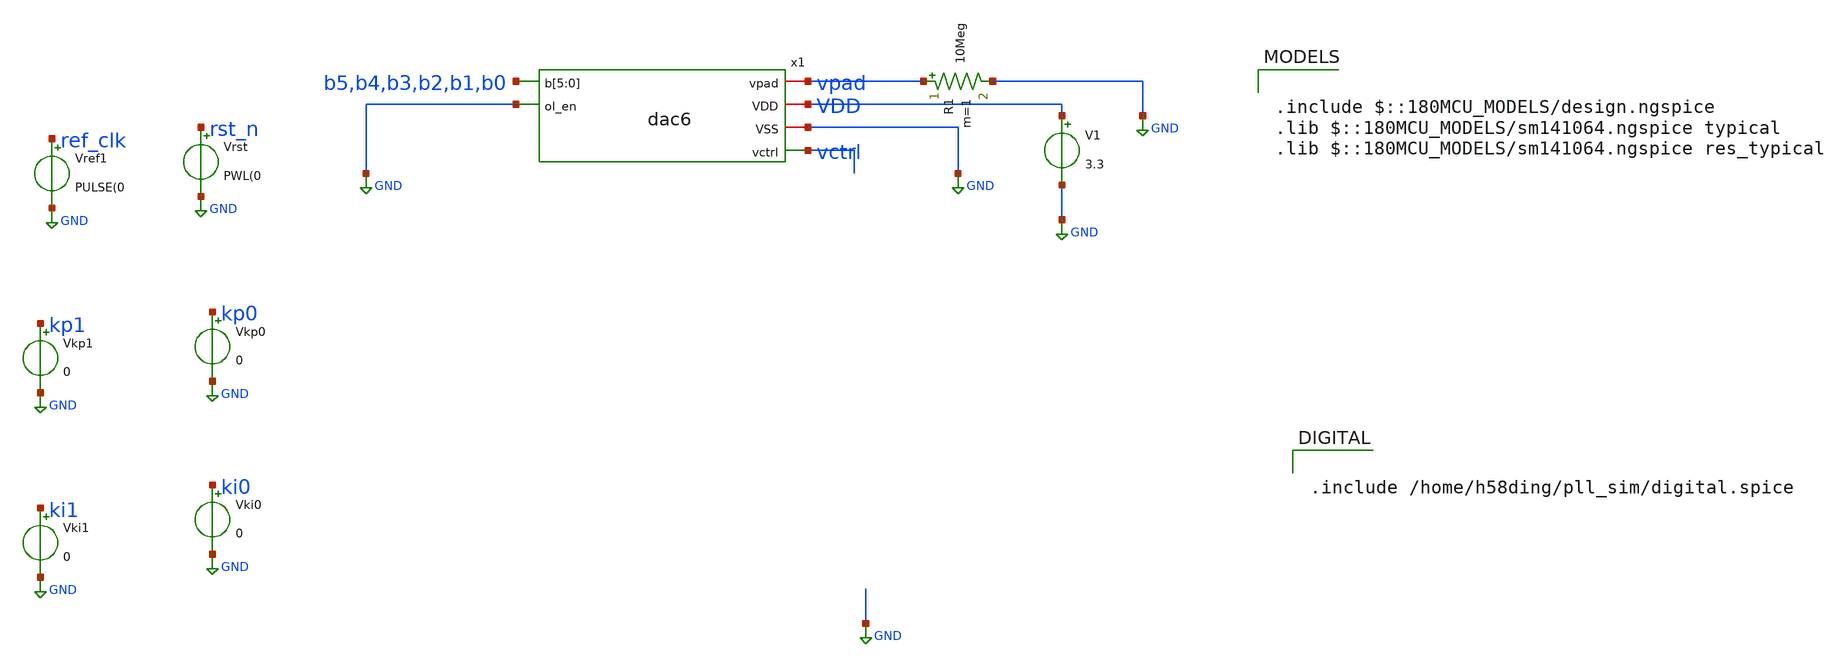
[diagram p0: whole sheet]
** sch_path: xschem/pll_dac/tb_pll.sch
**.subckt tb_pll
x1 b5 b4 b3 b2 b1 b0 GND vpad VDD GND vctrl dac6
V1 VDD GND 3.3
R1 vpad GND 10Meg m=1
Vrst rst_n GND PWL(0
Vref1 ref_clk GND PULSE(0
Vkp0 kp0 GND 0
Vkp1 kp1 GND 0
Vki0 ki0 GND 0
Vki1 ki1 GND 0
**** begin user architecture code

.include $::180MCU_MODELS/design.ngspice
.lib $::180MCU_MODELS/sm141064.ngspice typical
.lib $::180MCU_MODELS/sm141064.ngspice res_typical



.control
save v(vctrl) v(lock) v(clk_out) v(ref_clk) v(vco_out) v(b5) v(b4) v(b3) v(b2) v(b1) v(b0)
tran 0.1n 5u
let code = (32*v(b5) + 16*v(b4) + 8*v(b3) + 4*v(b2) + 2*v(b1) + v(b0)) / 3.3
plot code
plot v(vctrl)
plot v(ref_clk) v(clk_out)
.endc




.include /home/h58ding/pll_sim/digital.spice


**** end user architecture code
**.ends

* expanding   symbol:  pll_dac/dac6.sym # of pins=6
** sym_path: xschem/pll_dac/dac6.sym
** sch_path: xschem/pll_dac/dac6.sch
.subckt dac6 b[5] b[4] b[3] b[2] b[1] b[0] ol_en vpad VDD VSS vctrl
*.ipin b[5],b[4],b[3],b[2],b[1],b[0]
*.ipin ol_en
*.iopin vpad
*.iopin VDD
*.iopin VSS
*.opin vctrl
x1 VDD b[5] b[4] b[3] b[2] b[1] b[0] VSS vctrl schr2r6
XRD1 rd vctrl VSS ppolyf_u_1k r_width=1u r_length=61u m=1
XRD2[1] VSS rd VSS ppolyf_u_1k r_width=1u r_length=61u m=1
XRD2[0] VSS rd VSS ppolyf_u_1k r_width=1u r_length=61u m=1
XOL VDD ol_en ol_en_b VSS sw_inv
XM2 vctrl ol_en_b vpad VDD pfet_03v3 L=0.28u W=5.6u nf=1 ad='int((nf+1)/2) * W/nf * 0.18u' as='int((nf+2)/2) * W/nf * 0.18u'
+ pd='2*int((nf+1)/2) * (W/nf + 0.18u)' ps='2*int((nf+2)/2) * (W/nf + 0.18u)' nrd='0.18u / W' nrs='0.18u / W'
+ sa=0 sb=0 sd=0 m=1
XM1 vctrl ol_en vpad VSS nfet_03v3 L=0.28u W=2u nf=1 ad='int((nf+1)/2) * W/nf * 0.18u' as='int((nf+2)/2) * W/nf * 0.18u'
+ pd='2*int((nf+1)/2) * (W/nf + 0.18u)' ps='2*int((nf+2)/2) * (W/nf + 0.18u)' nrd='0.18u / W' nrs='0.18u / W'
+ sa=0 sb=0 sd=0 m=1
.ends


* expanding   symbol:  pll_dac/schr2r6.sym # of pins=4
** sym_path: xschem/pll_dac/schr2r6.sym
** sch_path: xschem/pll_dac/schr2r6.sch
.subckt schr2r6 VDD b[5] b[4] b[3] b[2] b[1] b[0] VSS lad
*.iopin VDD
*.iopin VSS
*.ipin b[5],b[4],b[3],b[2],b[1],b[0]
*.opin lad
XI[5] VDD b[5] d[5] VSS sw_inv
XI[4] VDD b[4] d[4] VSS sw_inv
XI[3] VDD b[3] d[3] VSS sw_inv
XI[2] VDD b[2] d[2] VSS sw_inv
XI[1] VDD b[1] d[1] VSS sw_inv
XI[0] VDD b[0] d[0] VSS sw_inv
XIT VDD VDD dt VSS sw_inv
XRLa[5] m[5] d[5] VSS ppolyf_u_1k r_width=1u r_length=61u m=1
XRLa[4] m[4] d[4] VSS ppolyf_u_1k r_width=1u r_length=61u m=1
XRLa[3] m[3] d[3] VSS ppolyf_u_1k r_width=1u r_length=61u m=1
XRLa[2] m[2] d[2] VSS ppolyf_u_1k r_width=1u r_length=61u m=1
XRLa[1] m[1] d[1] VSS ppolyf_u_1k r_width=1u r_length=61u m=1
XRLa[0] m[0] d[0] VSS ppolyf_u_1k r_width=1u r_length=61u m=1
XRLb[5] lad m[5] VSS ppolyf_u_1k r_width=1u r_length=61u m=1
XRLb[4] j[4] m[4] VSS ppolyf_u_1k r_width=1u r_length=61u m=1
XRLb[3] j[3] m[3] VSS ppolyf_u_1k r_width=1u r_length=61u m=1
XRLb[2] j[2] m[2] VSS ppolyf_u_1k r_width=1u r_length=61u m=1
XRLb[1] j[1] m[1] VSS ppolyf_u_1k r_width=1u r_length=61u m=1
XRLb[0] j[0] m[0] VSS ppolyf_u_1k r_width=1u r_length=61u m=1
XRR[4] lad j[4] VSS ppolyf_u_1k r_width=1u r_length=61u m=1
XRR[3] j[4] j[3] VSS ppolyf_u_1k r_width=1u r_length=61u m=1
XRR[2] j[3] j[2] VSS ppolyf_u_1k r_width=1u r_length=61u m=1
XRR[1] j[2] j[1] VSS ppolyf_u_1k r_width=1u r_length=61u m=1
XRR[0] j[1] j[0] VSS ppolyf_u_1k r_width=1u r_length=61u m=1
XRTa mt dt VSS ppolyf_u_1k r_width=1u r_length=61u m=1
XRTb j[0] mt VSS ppolyf_u_1k r_width=1u r_length=61u m=1
XRDUM[3] VSS VSS VSS ppolyf_u_1k r_width=1u r_length=61u m=1
XRDUM[2] VSS VSS VSS ppolyf_u_1k r_width=1u r_length=61u m=1
XRDUM[1] VSS VSS VSS ppolyf_u_1k r_width=1u r_length=61u m=1
XRDUM[0] VSS VSS VSS ppolyf_u_1k r_width=1u r_length=61u m=1
.ends


* expanding   symbol:  pll_dac/sw_inv.sym # of pins=4
** sym_path: xschem/pll_dac/sw_inv.sym
** sch_path: xschem/pll_dac/sw_inv.sch
.subckt sw_inv VDD A Y VSS
*.ipin A
*.iopin VDD
*.iopin VSS
*.opin Y
XM1 Y A VSS VSS nfet_03v3 L=0.28u W=2u nf=1 ad='int((nf+1)/2) * W/nf * 0.18u' as='int((nf+2)/2) * W/nf * 0.18u'
+ pd='2*int((nf+1)/2) * (W/nf + 0.18u)' ps='2*int((nf+2)/2) * (W/nf + 0.18u)' nrd='0.18u / W' nrs='0.18u / W'
+ sa=0 sb=0 sd=0 m=1
XM2 Y A VDD VDD pfet_03v3 L=0.28u W=5.6u nf=1 ad='int((nf+1)/2) * W/nf * 0.18u' as='int((nf+2)/2) * W/nf * 0.18u'
+ pd='2*int((nf+1)/2) * (W/nf + 0.18u)' ps='2*int((nf+2)/2) * (W/nf + 0.18u)' nrd='0.18u / W' nrs='0.18u / W'
+ sa=0 sb=0 sd=0 m=1
.ends

.GLOBAL GND
.end
